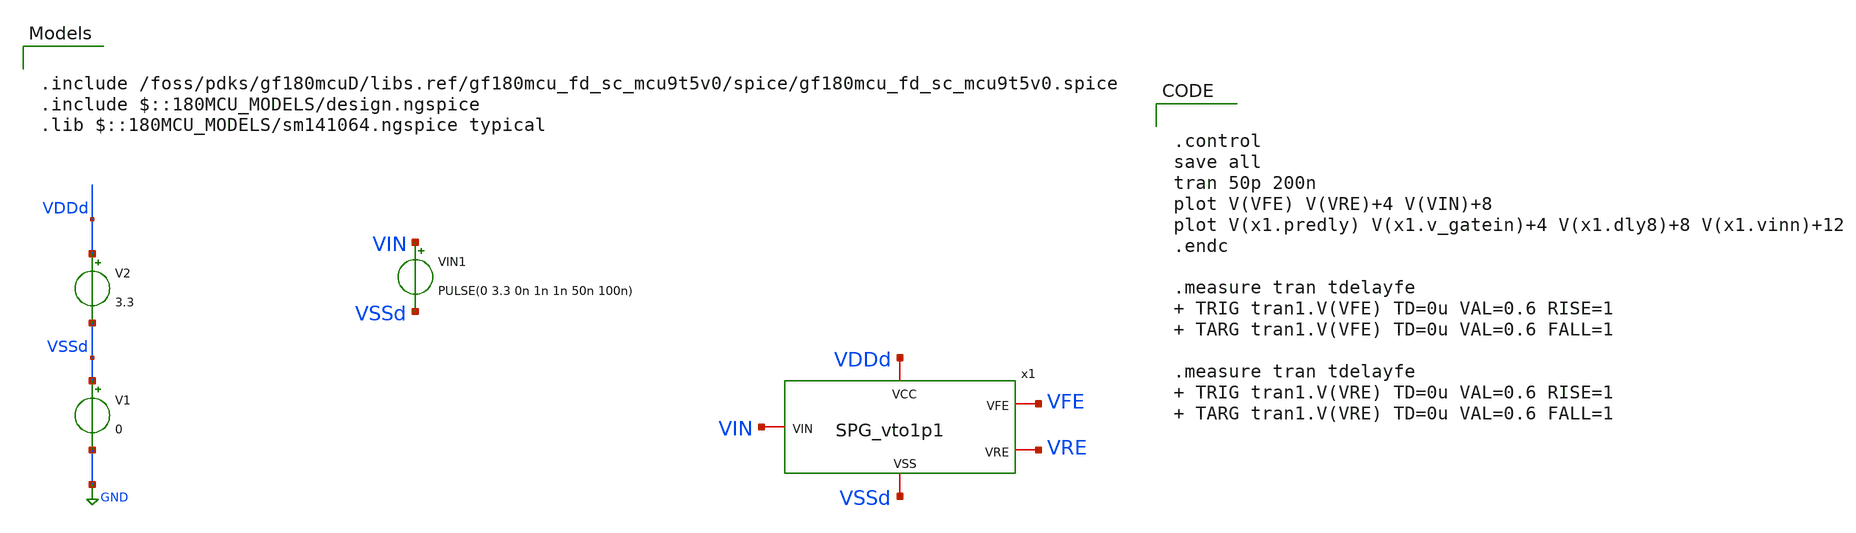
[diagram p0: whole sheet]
** sch_path: xschem/gf180_digital/SPG/tb_SPG_vto1p1.sch
**.subckt tb_SPG_vto1p1
x1 VDDd VSSd VFE VIN VRE SPG_vto1p1
VIN1 VIN VSSd PULSE(0 3.3 0n 1n 1n 50n 100n)
V1 VSSd GND 0
V2 VDDd VSSd 3.3
**** begin user architecture code


.control
save all
tran 50p 200n
plot V(VFE) V(VRE)+4 V(VIN)+8
plot V(x1.predly) V(x1.v_gatein)+4 V(x1.dly8)+8 V(x1.vinn)+12
.endc

.measure tran tdelayfe  TRIG tran1.V(VFE) TD=0u VAL=0.6 RISE=1  TARG tran1.V(VFE) TD=0u VAL=0.6
+ FALL=1

.measure tran tdelayfe  TRIG tran1.V(VRE) TD=0u VAL=0.6 RISE=1  TARG tran1.V(VRE) TD=0u VAL=0.6
+ FALL=1



.include /foss/pdks/gf180mcuD/libs.ref/gf180mcu_fd_sc_mcu9t5v0/spice/gf180mcu_fd_sc_mcu9t5v0.spice
.include $::180MCU_MODELS/design.ngspice
.lib $::180MCU_MODELS/sm141064.ngspice typical

**** end user architecture code
**.ends

* expanding   symbol:  gf180_digital/SPG/SPG_vto1p1.sym # of pins=5
** sym_path: xschem/gf180_digital/SPG/SPG_vto1p1.sym
** sch_path: xschem/gf180_digital/SPG/SPG_vto1p1.sch
.subckt SPG_vto1p1 VDDd VSSd VFE VIN VRE
*.iopin VIN
*.iopin VFE
*.iopin VRE
*.iopin VDDd
*.iopin VSSd
x2 predly VSSd VDDd VSSd VDDd net2 gf180mcu_fd_sc_mcu9t5v0__inv_1
x3 vinn VSSd VDDd VSSd VDDd predly gf180mcu_fd_sc_mcu9t5v0__inv_1
x4 dly8 VSSd VDDd VSSd VDDd net1 gf180mcu_fd_sc_mcu9t5v0__inv_1
x5 VIN VSSd VDDd VSSd VDDd vinn gf180mcu_fd_sc_mcu9t5v0__inv_2
x6 predly VSSd VDDd VSSd VDDd V_gatein gf180mcu_fd_sc_mcu9t5v0__inv_8
x9 VDDd VSSd V_gatein dly7 large_delay_vto1p1
x1 dly7 VSSd VDDd VSSd VDDd dly8 gf180mcu_fd_sc_mcu9t5v0__inv_8
x8 net2 dly8 VFE VDDd VDDd VSSd VSSd gf180mcu_fd_sc_mcu9t5v0__and2_1
x7 net1 predly VRE VDDd VDDd VSSd VSSd gf180mcu_fd_sc_mcu9t5v0__and2_1
.ends


* expanding   symbol:  gf180_digital/large_delay/large_delay_vto1p1.sym # of pins=4
** sym_path: xschem/gf180_digital/large_delay/large_delay_vto1p1.sym
** sch_path: xschem/gf180_digital/large_delay/large_delay_vto1p1.sch
.subckt large_delay_vto1p1 VDDd VSSd VIN VOUT
*.iopin VIN
*.iopin VOUT
*.iopin VDDd
*.iopin VSSd
x1 VIN VOUT VDDd VDDd VSSd VSSd gf180mcu_fd_sc_mcu9t5v0__dlya_1
.ends

.GLOBAL GND
.end
